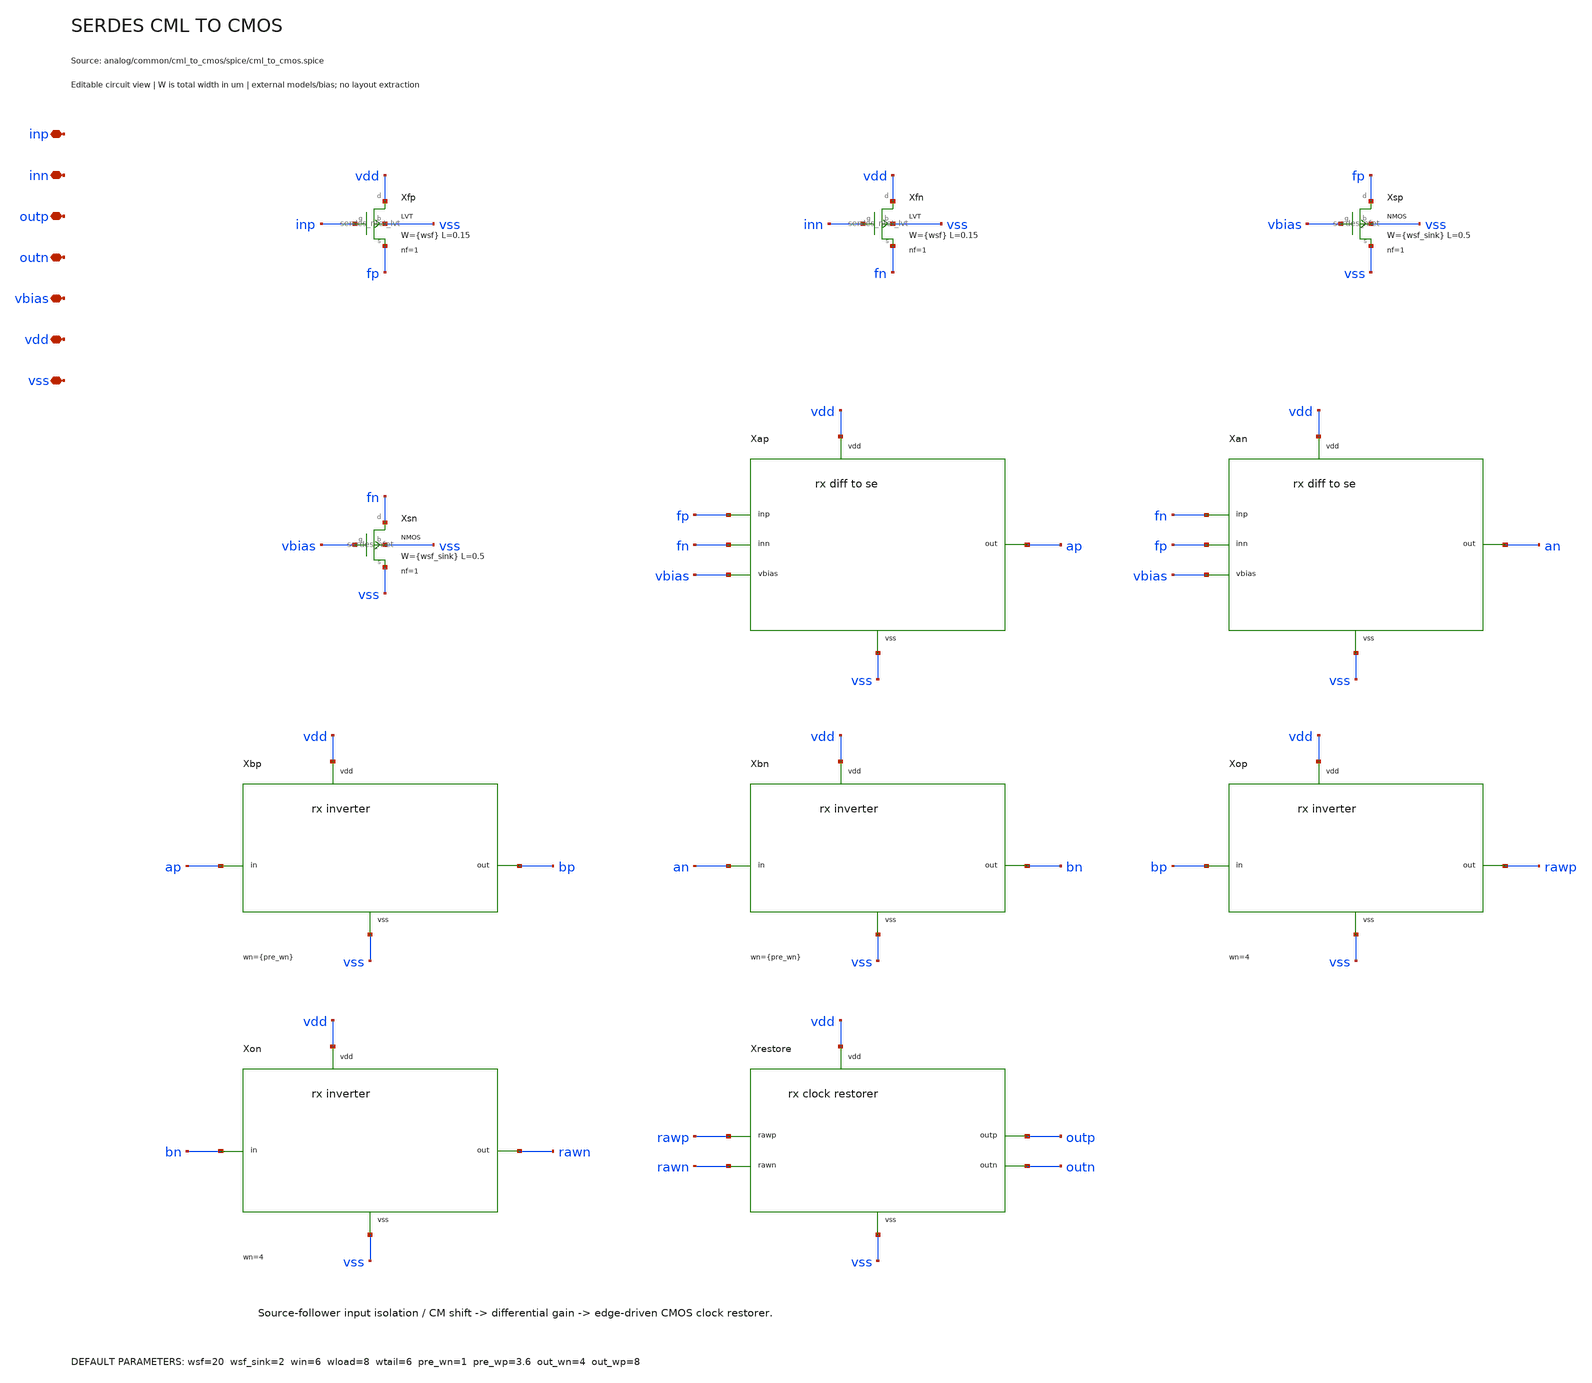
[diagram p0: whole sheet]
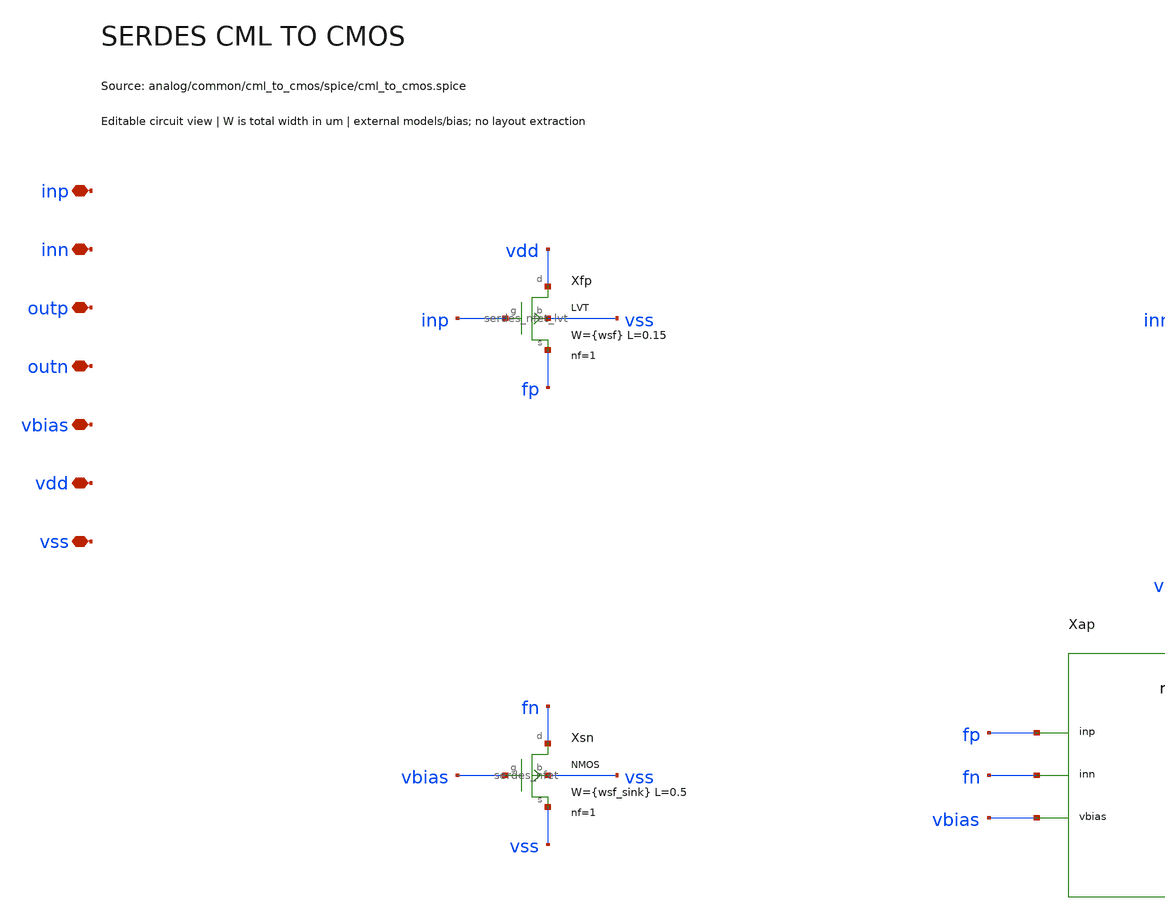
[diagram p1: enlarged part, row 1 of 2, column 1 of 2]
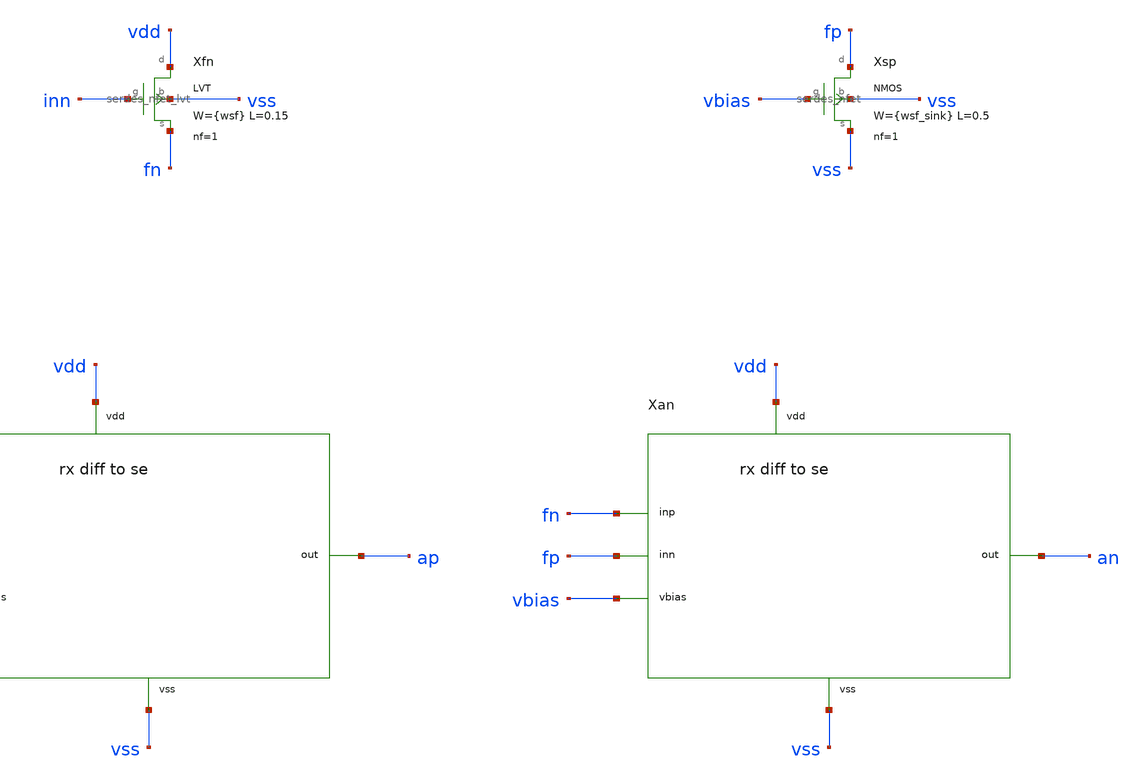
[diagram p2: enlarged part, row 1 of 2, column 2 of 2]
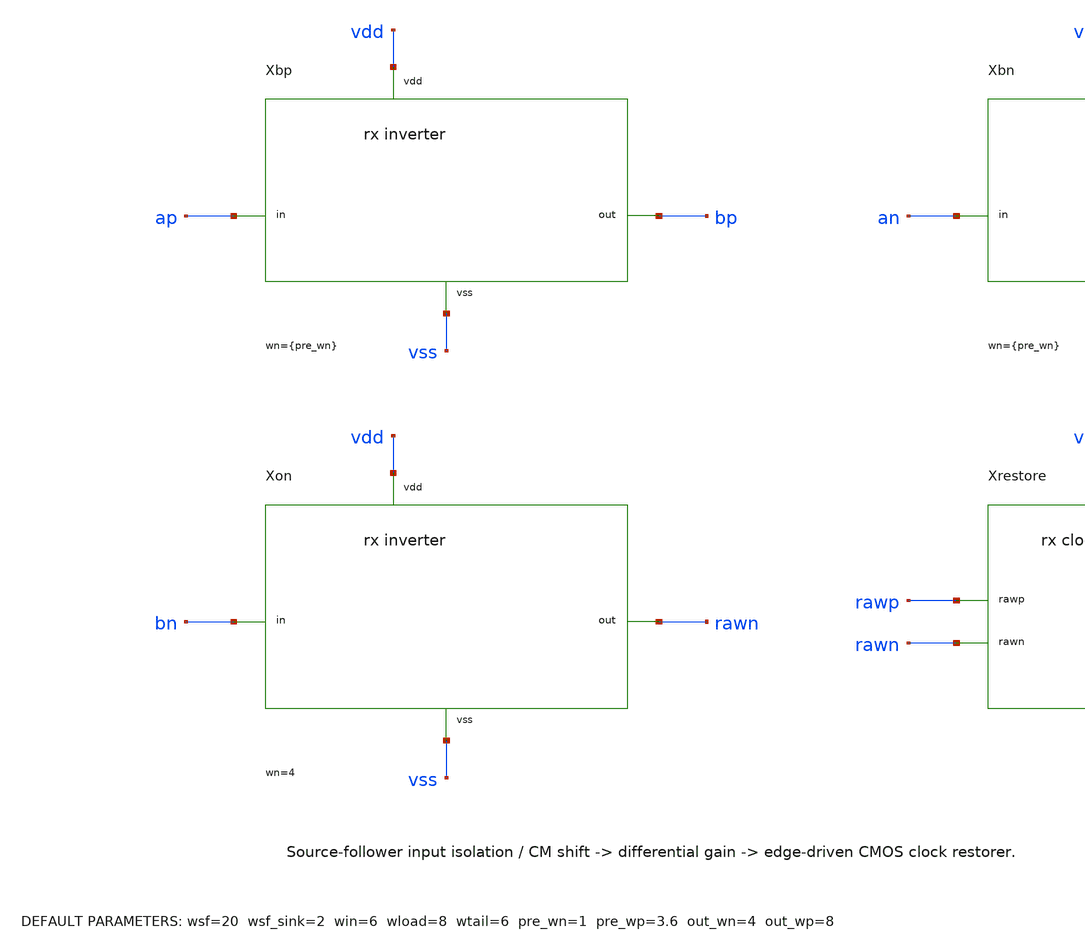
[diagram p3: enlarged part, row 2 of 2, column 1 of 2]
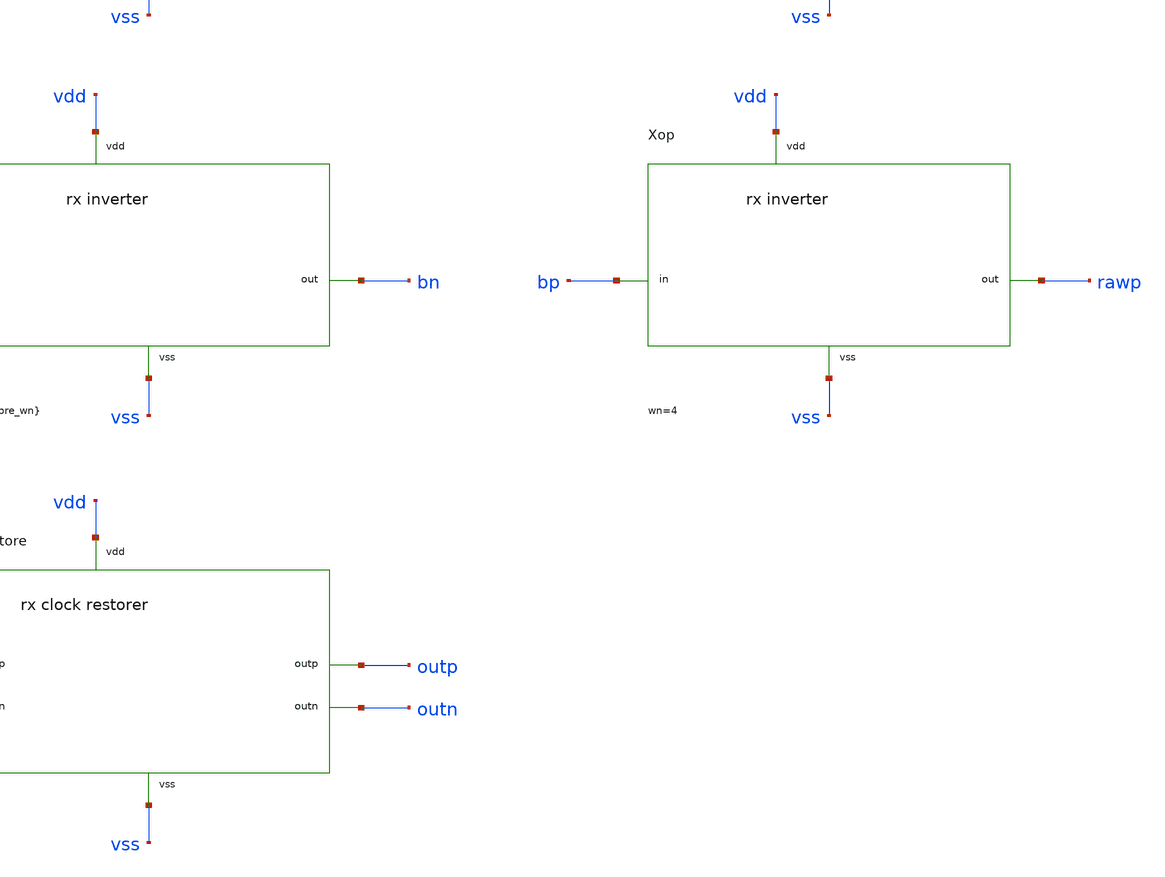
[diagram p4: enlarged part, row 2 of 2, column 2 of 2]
** sch_path: analog/common/cml_to_cmos/schematic/serdes_cml_to_cmos.sch
**.subckt serdes_cml_to_cmos inp inn outp outn vbias vdd vss
*.iopin inp
*.iopin inn
*.iopin outp
*.iopin outn
*.iopin vbias
*.iopin vdd
*.iopin vss
Xfp vdd inp fp vss serdes_nfet_lvt w={wsf} l=0.15 nf=1
Xfn vdd inn fn vss serdes_nfet_lvt w={wsf} l=0.15 nf=1
Xsp fp vbias vss vss serdes_nfet w={wsf_sink} l=0.5 nf=1
Xsn fn vbias vss vss serdes_nfet w={wsf_sink} l=0.5 nf=1
Xap fp fn ap vbias vdd vss serdes_rx_diff_to_se win={win} nfin=1 wload={wload} nfload=2 wtail={wtail}
Xan fn fp an vbias vdd vss serdes_rx_diff_to_se win={win} nfin=1 wload={wload} nfload=2 wtail={wtail}
Xbp ap bp vdd vss serdes_rx_inverter wn={pre_wn} wp={pre_wp} nfn=1 nfp=1
Xbn an bn vdd vss serdes_rx_inverter wn={pre_wn} wp={pre_wp} nfn=1 nfp=1
Xop bp rawp vdd vss serdes_rx_inverter wn=4 wp=12 nfn=1 nfp=4
Xon bn rawn vdd vss serdes_rx_inverter wn=4 wp=12 nfn=1 nfp=4
Xrestore rawp rawn outp outn vdd vss serdes_rx_clock_restorer out_wn={out_wn} out_wp={out_wp}
**.ends

* expanding   symbol:  serdes/serdes_nfet_lvt.sym # of pins=4
** sym_path: analog/common/devices/schematic/serdes_nfet_lvt.sym
** sch_path: analog/common/devices/schematic/serdes_nfet_lvt.sch
.subckt serdes_nfet_lvt d g s b  w=1 l=0.15 nf=1
*.iopin d
*.iopin g
*.iopin s
*.iopin b
Xmos d g s b sky130_fd_pr__nfet_01v8_lvt w={w} l={l} nf={nf} ad={floor((nf+1)/2)*(w/nf)*0.29} as={floor((nf+2)/2)*(w/nf)*0.29}
+ pd={2*floor((nf+1)/2)*(w/nf+0.29)} ps={2*floor((nf+2)/2)*(w/nf+0.29)}
.ends


* expanding   symbol:  serdes/serdes_nfet.sym # of pins=4
** sym_path: analog/common/devices/schematic/serdes_nfet.sym
** sch_path: analog/common/devices/schematic/serdes_nfet.sch
.subckt serdes_nfet d g s b  w=1 l=0.15 nf=1
*.iopin d
*.iopin g
*.iopin s
*.iopin b
Xmos d g s b sky130_fd_pr__nfet_01v8 w={w} l={l} nf={nf} ad={floor((nf+1)/2)*(w/nf)*0.29} as={floor((nf+2)/2)*(w/nf)*0.29}
+ pd={2*floor((nf+1)/2)*(w/nf+0.29)} ps={2*floor((nf+2)/2)*(w/nf+0.29)}
.ends


* expanding   symbol:  serdes/serdes_rx_diff_to_se.sym # of pins=6
** sym_path: analog/common/cml_to_cmos/schematic/serdes_rx_diff_to_se.sym
** sch_path: analog/common/cml_to_cmos/schematic/serdes_rx_diff_to_se.sch
.subckt serdes_rx_diff_to_se inp inn out vbias vdd vss  win=6 nfin=1 wload=8 nfload=2 wtail=6
*.iopin inp
*.iopin inn
*.iopin out
*.iopin vbias
*.iopin vdd
*.iopin vss
Xip mirror inp tail vss serdes_nfet_lvt w={win} l=0.15 nf={nfin}
Xin out inn tail vss serdes_nfet_lvt w={win} l=0.15 nf={nfin}
Xlp mirror mirror vdd vdd serdes_pfet w={wload} l=0.15 nf={nfload}
Xln out mirror vdd vdd serdes_pfet w={wload} l=0.15 nf={nfload}
Xtail tail vbias vss vss serdes_nfet w={wtail} l=0.5 nf=1
.ends


* expanding   symbol:  serdes/serdes_rx_inverter.sym # of pins=4
** sym_path: analog/common/cml_to_cmos/schematic/serdes_rx_inverter.sym
** sch_path: analog/common/cml_to_cmos/schematic/serdes_rx_inverter.sch
.subckt serdes_rx_inverter in out vdd vss  wn=1 wp=3 nfn=1 nfp=1
*.iopin in
*.iopin out
*.iopin vdd
*.iopin vss
Xn out in vss vss serdes_nfet w={wn} l=0.15 nf={nfn}
Xp out in vdd vdd serdes_pfet w={wp} l=0.15 nf={nfp}
.ends


* expanding   symbol:  serdes/serdes_rx_clock_restorer.sym # of pins=6
** sym_path: analog/common/cml_to_cmos/schematic/serdes_rx_clock_restorer.sym
** sch_path: analog/common/cml_to_cmos/schematic/serdes_rx_clock_restorer.sch
.subckt serdes_rx_clock_restorer rawp rawn outp outn vdd vss  out_wn=4 out_wp=8
*.iopin rawp
*.iopin rawn
*.iopin outp
*.iopin outn
*.iopin vdd
*.iopin vss
Xdp1 rawp dp1 vdd vss serdes_rx_inverter wn=0.5 wp=1.5 nfn=1 nfp=1
Xdp2 dp1 dp2 vdd vss serdes_rx_inverter wn=0.5 wp=1.5 nfn=1 nfp=1
Xdp3 dp2 dp3 vdd vss serdes_rx_inverter wn=0.5 wp=1.5 nfn=1 nfp=1
Xdn1 rawn dn1 vdd vss serdes_rx_inverter wn=0.5 wp=1.5 nfn=1 nfp=1
Xdn2 dn1 dn2 vdd vss serdes_rx_inverter wn=0.5 wp=1.5 nfn=1 nfp=1
Xdn3 dn2 dn3 vdd vss serdes_rx_inverter wn=0.5 wp=1.5 nfn=1 nfp=1
Xset rawp dp3 set_b vdd vss serdes_rx_nand2 wn=2 wp=3
Xreset rawn dn3 reset_b vdd vss serdes_rx_nand2 wn=2 wp=3
Xqp set_b qn qp vdd vss serdes_rx_nand2 wn=4 wp=6
Xqn reset_b qp qn vdd vss serdes_rx_nand2 wn=4 wp=6
Xrp1 qp rp1 vdd vss serdes_rx_inverter wn=2 wp=6 nfn=1 nfp=1
Xrp2 rp1 rp2 vdd vss serdes_rx_inverter wn=1 wp=3 nfn=1 nfp=1
Xrn1 qn rn1 vdd vss serdes_rx_inverter wn=2 wp=6 nfn=1 nfp=1
Xrn2 rn1 rn2 vdd vss serdes_rx_inverter wn=1 wp=3 nfn=1 nfp=1
Xbp qp rp2 bp vdd vss serdes_rx_nand2 wn=2 wp=3
Xbn qn rn2 bn vdd vss serdes_rx_nand2 wn=2 wp=3
Xop bp outp vdd vss serdes_rx_inverter wn={out_wn} wp={out_wp} nfn=1 nfp=4
Xon bn outn vdd vss serdes_rx_inverter wn={out_wn} wp={out_wp} nfn=1 nfp=4
.ends


* expanding   symbol:  serdes/serdes_pfet.sym # of pins=4
** sym_path: analog/common/devices/schematic/serdes_pfet.sym
** sch_path: analog/common/devices/schematic/serdes_pfet.sch
.subckt serdes_pfet d g s b  w=3 l=0.15 nf=1
*.iopin d
*.iopin g
*.iopin s
*.iopin b
Xmos d g s b sky130_fd_pr__pfet_01v8 w={w} l={l} nf={nf} ad={floor((nf+1)/2)*(w/nf)*0.29} as={floor((nf+2)/2)*(w/nf)*0.29}
+ pd={2*floor((nf+1)/2)*(w/nf+0.29)} ps={2*floor((nf+2)/2)*(w/nf+0.29)}
.ends


* expanding   symbol:  serdes/serdes_rx_nand2.sym # of pins=5
** sym_path: analog/common/cml_to_cmos/schematic/serdes_rx_nand2.sym
** sch_path: analog/common/cml_to_cmos/schematic/serdes_rx_nand2.sch
.subckt serdes_rx_nand2 a b out vdd vss  wn=2 wp=3
*.iopin a
*.iopin b
*.iopin out
*.iopin vdd
*.iopin vss
Xnt out a mid vss serdes_nfet w={wn} l=0.15 nf=1
Xnb mid b vss vss serdes_nfet w={wn} l=0.15 nf=1
Xpa out a vdd vdd serdes_pfet w={wp} l=0.15 nf=1
Xpb out b vdd vdd serdes_pfet w={wp} l=0.15 nf=1
.ends

.end
